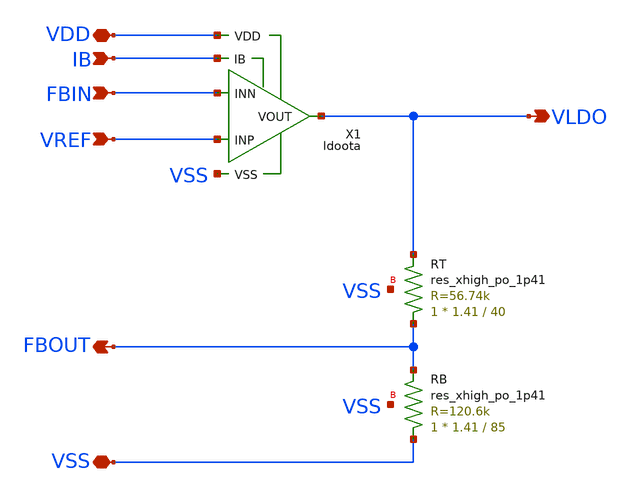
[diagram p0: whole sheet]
** sch_path: tt08/ip/ldo/xschem/ldo.sch
**.subckt ldo VSS VDD VLDO VREF FBOUT FBIN IB
*.iopin VSS
*.iopin VDD
*.opin VLDO
*.ipin VREF
*.opin FBOUT
*.ipin FBIN
*.ipin IB
XRT FBOUT VLDO VSS sky130_fd_pr__res_xhigh_po_1p41 L=40 mult=1 m=1
X1 VDD VSS VLDO IB FBIN VREF ldoota
XRB VSS FBOUT VSS sky130_fd_pr__res_xhigh_po_1p41 L=85 mult=1 m=1
**.ends

* expanding   symbol:  ldoota.sym # of pins=6
** sym_path: ldoota.sym
** sch_path: ldoota.sch
.subckt ldoota VDD VSS VOUT IB INN INP
*.ipin IB
*.iopin VDD
*.iopin VSS
*.iopin INP
*.iopin INN
*.iopin VOUT
XMMIRL net1 net1 VDD VDD sky130_fd_pr__pfet_g5v0d10v5 L=2 W=20 nf=1 ad='int((nf+1)/2) * W/nf * 0.29'
+ as='int((nf+2)/2) * W/nf * 0.29' pd='2*int((nf+1)/2) * (W/nf + 0.29)' ps='2*int((nf+2)/2) * (W/nf + 0.29)'
+ nrd='0.29 / W' nrs='0.29 / W' sa=0 sb=0 sd=0 mult=1 m=1
XMMIRR net2 net2 VDD VDD sky130_fd_pr__pfet_g5v0d10v5 L=2 W=20 nf=1 ad='int((nf+1)/2) * W/nf * 0.29'
+ as='int((nf+2)/2) * W/nf * 0.29' pd='2*int((nf+1)/2) * (W/nf + 0.29)' ps='2*int((nf+2)/2) * (W/nf + 0.29)'
+ nrd='0.29 / W' nrs='0.29 / W' sa=0 sb=0 sd=0 mult=1 m=1
XMDR net2 INN net3 VSS sky130_fd_pr__nfet_g5v0d10v5 L=2 W=20 nf=1 ad='int((nf+1)/2) * W/nf * 0.29' as='int((nf+2)/2) * W/nf * 0.29'
+ pd='2*int((nf+1)/2) * (W/nf + 0.29)' ps='2*int((nf+2)/2) * (W/nf + 0.29)' nrd='0.29 / W' nrs='0.29 / W'
+ sa=0 sb=0 sd=0 mult=5 m=5
XMDL net1 INP net3 VSS sky130_fd_pr__nfet_g5v0d10v5 L=2 W=20 nf=1 ad='int((nf+1)/2) * W/nf * 0.29' as='int((nf+2)/2) * W/nf * 0.29'
+ pd='2*int((nf+1)/2) * (W/nf + 0.29)' ps='2*int((nf+2)/2) * (W/nf + 0.29)' nrd='0.29 / W' nrs='0.29 / W'
+ sa=0 sb=0 sd=0 mult=5 m=5
XMMIR2 net3 IB VSS VSS sky130_fd_pr__nfet_g5v0d10v5 L=2 W=20 nf=1 ad='int((nf+1)/2) * W/nf * 0.29' as='int((nf+2)/2) * W/nf * 0.29'
+ pd='2*int((nf+1)/2) * (W/nf + 0.29)' ps='2*int((nf+2)/2) * (W/nf + 0.29)' nrd='0.29 / W' nrs='0.29 / W'
+ sa=0 sb=0 sd=0 mult=1 m=1
XMO vot net2 VDD VDD sky130_fd_pr__pfet_g5v0d10v5 L=2 W=20 nf=1 ad='int((nf+1)/2) * W/nf * 0.29' as='int((nf+2)/2) * W/nf * 0.29'
+ pd='2*int((nf+1)/2) * (W/nf + 0.29)' ps='2*int((nf+2)/2) * (W/nf + 0.29)' nrd='0.29 / W' nrs='0.29 / W'
+ sa=0 sb=0 sd=0 mult=5 m=5
XMMIRL1 net4 net1 VDD VDD sky130_fd_pr__pfet_g5v0d10v5 L=2 W=20 nf=1 ad='int((nf+1)/2) * W/nf * 0.29'
+ as='int((nf+2)/2) * W/nf * 0.29' pd='2*int((nf+1)/2) * (W/nf + 0.29)' ps='2*int((nf+2)/2) * (W/nf + 0.29)'
+ nrd='0.29 / W' nrs='0.29 / W' sa=0 sb=0 sd=0 mult=1 m=1
XMMIRL2 net4 net4 VSS VSS sky130_fd_pr__nfet_g5v0d10v5 L=2 W=20 nf=1 ad='int((nf+1)/2) * W/nf * 0.29'
+ as='int((nf+2)/2) * W/nf * 0.29' pd='2*int((nf+1)/2) * (W/nf + 0.29)' ps='2*int((nf+2)/2) * (W/nf + 0.29)'
+ nrd='0.29 / W' nrs='0.29 / W' sa=0 sb=0 sd=0 mult=1 m=1
XMMIR3 vot net4 VSS VSS sky130_fd_pr__nfet_g5v0d10v5 L=2 W=20 nf=1 ad='int((nf+1)/2) * W/nf * 0.29' as='int((nf+2)/2) * W/nf * 0.29'
+ pd='2*int((nf+1)/2) * (W/nf + 0.29)' ps='2*int((nf+2)/2) * (W/nf + 0.29)' nrd='0.29 / W' nrs='0.29 / W'
+ sa=0 sb=0 sd=0 mult=5 m=5
XMOT VOUT vot VDD VDD sky130_fd_pr__pfet_g5v0d10v5 L=0.5 W=20 nf=1 ad='int((nf+1)/2) * W/nf * 0.29' as='int((nf+2)/2) * W/nf * 0.29'
+ pd='2*int((nf+1)/2) * (W/nf + 0.29)' ps='2*int((nf+2)/2) * (W/nf + 0.29)' nrd='0.29 / W' nrs='0.29 / W'
+ sa=0 sb=0 sd=0 mult=20 m=20
XMOB VOUT IB VSS VSS sky130_fd_pr__nfet_g5v0d10v5 L=2 W=20 nf=1 ad='int((nf+1)/2) * W/nf * 0.29' as='int((nf+2)/2) * W/nf * 0.29'
+ pd='2*int((nf+1)/2) * (W/nf + 0.29)' ps='2*int((nf+2)/2) * (W/nf + 0.29)' nrd='0.29 / W' nrs='0.29 / W'
+ sa=0 sb=0 sd=0 mult=4 m=4
XC1 net5 vot sky130_fd_pr__cap_mim_m3_1 W=20 L=20 MF=16 m=16
XMMIR1 IB IB VSS VSS sky130_fd_pr__nfet_g5v0d10v5 L=2 W=20 nf=1 ad='int((nf+1)/2) * W/nf * 0.29' as='int((nf+2)/2) * W/nf * 0.29'
+ pd='2*int((nf+1)/2) * (W/nf + 0.29)' ps='2*int((nf+2)/2) * (W/nf + 0.29)' nrd='0.29 / W' nrs='0.29 / W'
+ sa=0 sb=0 sd=0 mult=1 m=1
XR1 net5 VOUT VSS sky130_fd_pr__res_xhigh_po_1p41 L=2 mult=1 m=1
XMMIRL3 VDD VDD VDD VDD sky130_fd_pr__pfet_g5v0d10v5 L=2 W=10 nf=1 ad='int((nf+1)/2) * W/nf * 0.29' as='int((nf+2)/2) * W/nf * 0.29'
+ pd='2*int((nf+1)/2) * (W/nf + 0.29)' ps='2*int((nf+2)/2) * (W/nf + 0.29)' nrd='0.29 / W' nrs='0.29 / W'
+ sa=0 sb=0 sd=0 mult=1 m=1
XMMIRL4 VDD VDD VDD VDD sky130_fd_pr__pfet_g5v0d10v5 L=2 W=10 nf=1 ad='int((nf+1)/2) * W/nf * 0.29' as='int((nf+2)/2) * W/nf * 0.29'
+ pd='2*int((nf+1)/2) * (W/nf + 0.29)' ps='2*int((nf+2)/2) * (W/nf + 0.29)' nrd='0.29 / W' nrs='0.29 / W'
+ sa=0 sb=0 sd=0 mult=1 m=1
XMMIRR1 VDD VDD VDD VDD sky130_fd_pr__pfet_g5v0d10v5 L=2 W=10 nf=1 ad='int((nf+1)/2) * W/nf * 0.29' as='int((nf+2)/2) * W/nf * 0.29'
+ pd='2*int((nf+1)/2) * (W/nf + 0.29)' ps='2*int((nf+2)/2) * (W/nf + 0.29)' nrd='0.29 / W' nrs='0.29 / W'
+ sa=0 sb=0 sd=0 mult=1 m=1
XMO1 VDD VDD VDD VDD sky130_fd_pr__pfet_g5v0d10v5 L=2 W=10 nf=1 ad='int((nf+1)/2) * W/nf * 0.29' as='int((nf+2)/2) * W/nf * 0.29'
+ pd='2*int((nf+1)/2) * (W/nf + 0.29)' ps='2*int((nf+2)/2) * (W/nf + 0.29)' nrd='0.29 / W' nrs='0.29 / W'
+ sa=0 sb=0 sd=0 mult=1 m=1
XMMIR4 VSS VSS VSS VSS sky130_fd_pr__nfet_g5v0d10v5 L=2 W=10 nf=1 ad='int((nf+1)/2) * W/nf * 0.29' as='int((nf+2)/2) * W/nf * 0.29'
+ pd='2*int((nf+1)/2) * (W/nf + 0.29)' ps='2*int((nf+2)/2) * (W/nf + 0.29)' nrd='0.29 / W' nrs='0.29 / W'
+ sa=0 sb=0 sd=0 mult=1 m=1
XMMIRL5 VSS VSS VSS VSS sky130_fd_pr__nfet_g5v0d10v5 L=2 W=10 nf=1 ad='int((nf+1)/2) * W/nf * 0.29' as='int((nf+2)/2) * W/nf * 0.29'
+ pd='2*int((nf+1)/2) * (W/nf + 0.29)' ps='2*int((nf+2)/2) * (W/nf + 0.29)' nrd='0.29 / W' nrs='0.29 / W'
+ sa=0 sb=0 sd=0 mult=1 m=1
XMDL1 VSS VSS VSS VSS sky130_fd_pr__nfet_g5v0d10v5 L=2 W=20 nf=1 ad='int((nf+1)/2) * W/nf * 0.29' as='int((nf+2)/2) * W/nf * 0.29'
+ pd='2*int((nf+1)/2) * (W/nf + 0.29)' ps='2*int((nf+2)/2) * (W/nf + 0.29)' nrd='0.29 / W' nrs='0.29 / W'
+ sa=0 sb=0 sd=0 mult=1 m=1
XMDR1 VSS VSS VSS VSS sky130_fd_pr__nfet_g5v0d10v5 L=2 W=20 nf=1 ad='int((nf+1)/2) * W/nf * 0.29' as='int((nf+2)/2) * W/nf * 0.29'
+ pd='2*int((nf+1)/2) * (W/nf + 0.29)' ps='2*int((nf+2)/2) * (W/nf + 0.29)' nrd='0.29 / W' nrs='0.29 / W'
+ sa=0 sb=0 sd=0 mult=1 m=1
XMMIR5 VSS VSS VSS VSS sky130_fd_pr__nfet_g5v0d10v5 L=2 W=10 nf=1 ad='int((nf+1)/2) * W/nf * 0.29' as='int((nf+2)/2) * W/nf * 0.29'
+ pd='2*int((nf+1)/2) * (W/nf + 0.29)' ps='2*int((nf+2)/2) * (W/nf + 0.29)' nrd='0.29 / W' nrs='0.29 / W'
+ sa=0 sb=0 sd=0 mult=1 m=1
XMOB1 VSS VSS VSS VSS sky130_fd_pr__nfet_g5v0d10v5 L=2 W=10 nf=1 ad='int((nf+1)/2) * W/nf * 0.29' as='int((nf+2)/2) * W/nf * 0.29'
+ pd='2*int((nf+1)/2) * (W/nf + 0.29)' ps='2*int((nf+2)/2) * (W/nf + 0.29)' nrd='0.29 / W' nrs='0.29 / W'
+ sa=0 sb=0 sd=0 mult=1 m=1
.ends

.end
